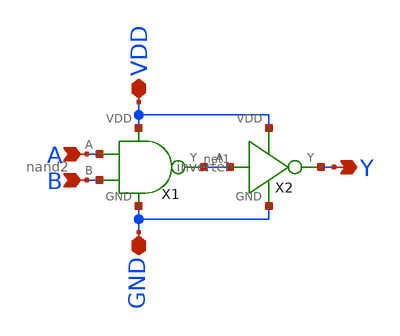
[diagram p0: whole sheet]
** sch_path: schematic/layout_driven_schematics/and2.sch
**.subckt and2 A B Y VDD GND
*.ipin A
*.ipin B
*.opin Y
*.iopin VDD
*.iopin GND
X1 A B net1 VDD GND nand2
X2 net1 Y VDD GND inverter
**.ends

* expanding   symbol:  /home/madvlsi/Documents/MP1/schematic/layout_driven_schematics/nand2.sym # of
*+ pins=5
** sym_path: schematic/layout_driven_schematics/nand2.sym
** sch_path: schematic/layout_driven_schematics/nand2.sch
.subckt nand2 A B Y VDD GND
*.ipin A
*.opin Y
*.ipin B
*.iopin VDD
*.iopin VDD
*.iopin GND
XM5 Y A VDD VDD sky130_fd_pr__pfet_01v8 L=0.15 W=2 nf=1 ad='int((nf+1)/2) * W/nf * 0.29' as='int((nf+2)/2) * W/nf * 0.29'
+ pd='2*int((nf+1)/2) * (W/nf + 0.29)' ps='2*int((nf+2)/2) * (W/nf + 0.29)' nrd='0.29 / W' nrs='0.29 / W'
+ sa=0 sb=0 sd=0 mult=1 m=1
XM6 VDD B Y VDD sky130_fd_pr__pfet_01v8 L=0.15 W=2 nf=1 ad='int((nf+1)/2) * W/nf * 0.29' as='int((nf+2)/2) * W/nf * 0.29'
+ pd='2*int((nf+1)/2) * (W/nf + 0.29)' ps='2*int((nf+2)/2) * (W/nf + 0.29)' nrd='0.29 / W' nrs='0.29 / W'
+ sa=0 sb=0 sd=0 mult=1 m=1
XM7 GND A net1 GND sky130_fd_pr__nfet_01v8 L=0.15 W=2 nf=1 ad='int((nf+1)/2) * W/nf * 0.29' as='int((nf+2)/2) * W/nf * 0.29'
+ pd='2*int((nf+1)/2) * (W/nf + 0.29)' ps='2*int((nf+2)/2) * (W/nf + 0.29)' nrd='0.29 / W' nrs='0.29 / W'
+ sa=0 sb=0 sd=0 mult=1 m=1
XM8 net1 B Y GND sky130_fd_pr__nfet_01v8 L=0.15 W=2 nf=1 ad='int((nf+1)/2) * W/nf * 0.29' as='int((nf+2)/2) * W/nf * 0.29'
+ pd='2*int((nf+1)/2) * (W/nf + 0.29)' ps='2*int((nf+2)/2) * (W/nf + 0.29)' nrd='0.29 / W' nrs='0.29 / W'
+ sa=0 sb=0 sd=0 mult=1 m=1
.ends


* expanding   symbol:  /home/madvlsi/Documents/MP1/schematic/layout_driven_schematics/inverter.sym #
*+ of pins=4
** sym_path: schematic/layout_driven_schematics/inverter.sym
** sch_path: schematic/layout_driven_schematics/inverter.sch
.subckt inverter A Y VDD GND
*.ipin A
*.iopin VDD
*.iopin GND
*.opin Y
XM3 Y A VDD VDD sky130_fd_pr__pfet_01v8 L=0.15 W=2 nf=1 ad='int((nf+1)/2) * W/nf * 0.29' as='int((nf+2)/2) * W/nf * 0.29'
+ pd='2*int((nf+1)/2) * (W/nf + 0.29)' ps='2*int((nf+2)/2) * (W/nf + 0.29)' nrd='0.29 / W' nrs='0.29 / W'
+ sa=0 sb=0 sd=0 mult=1 m=1
XM4 GND A Y GND sky130_fd_pr__nfet_01v8 L=0.15 W=2 nf=1 ad='int((nf+1)/2) * W/nf * 0.29' as='int((nf+2)/2) * W/nf * 0.29'
+ pd='2*int((nf+1)/2) * (W/nf + 0.29)' ps='2*int((nf+2)/2) * (W/nf + 0.29)' nrd='0.29 / W' nrs='0.29 / W'
+ sa=0 sb=0 sd=0 mult=1 m=1
.ends

.end
